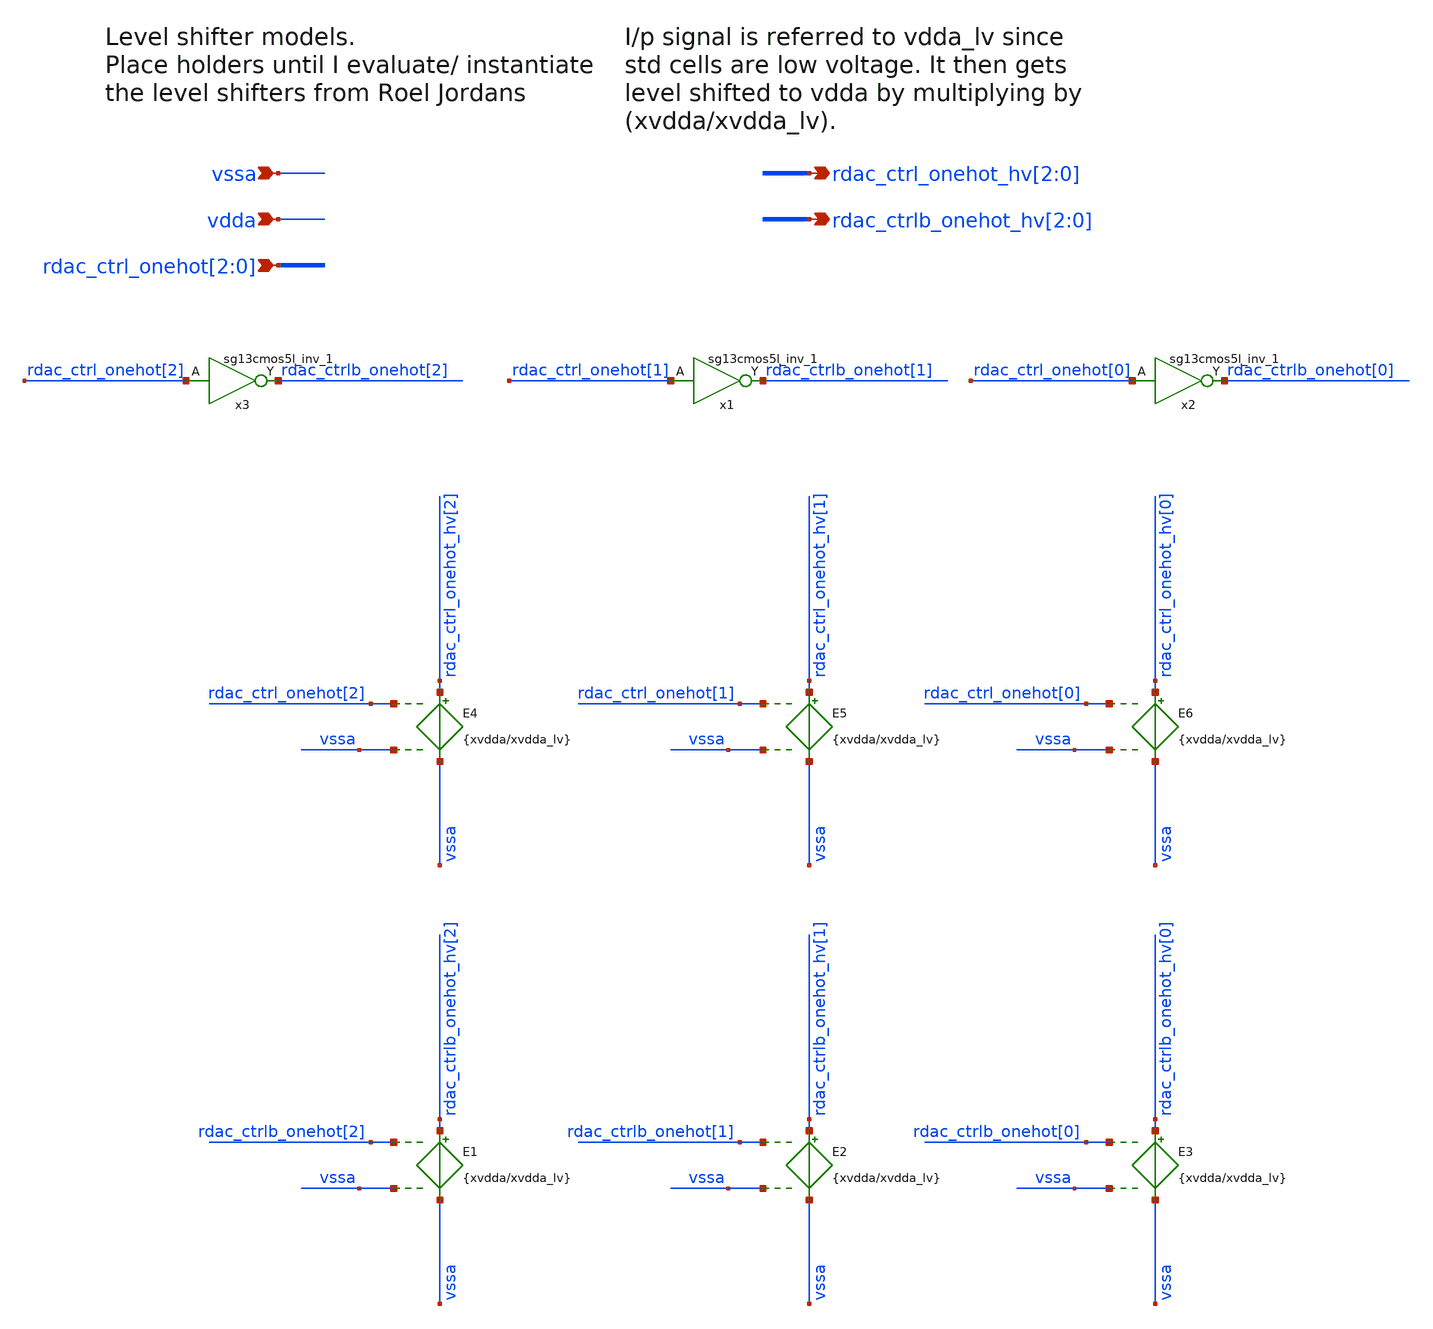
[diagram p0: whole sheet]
** sch_path: Design_Review_2/INA/Testbench_3_tb_sunrise_bias_ia_top_STEP_STB_NOISE/lvl_shfters.sch
**.subckt lvl_shfters rdac_ctrl_onehot[2],rdac_ctrl_onehot[1],rdac_ctrl_onehot[0] vssa
*+ rdac_ctrl_onehot_hv[2],rdac_ctrl_onehot_hv[1],rdac_ctrl_onehot_hv[0] rdac_ctrlb_onehot_hv[2],rdac_ctrlb_onehot_hv[1],rdac_ctrlb_onehot_hv[0] vdda
*.ipin rdac_ctrl_onehot[2],rdac_ctrl_onehot[1],rdac_ctrl_onehot[0]
*.ipin vssa
*.opin rdac_ctrl_onehot_hv[2],rdac_ctrl_onehot_hv[1],rdac_ctrl_onehot_hv[0]
*.opin rdac_ctrlb_onehot_hv[2],rdac_ctrlb_onehot_hv[1],rdac_ctrlb_onehot_hv[0]
*.ipin vdda
E1 rdac_ctrlb_onehot_hv[2] vssa rdac_ctrlb_onehot[2] vssa {xvdda/xvdda_lv}
E2 rdac_ctrlb_onehot_hv[1] vssa rdac_ctrlb_onehot[1] vssa {xvdda/xvdda_lv}
E3 rdac_ctrlb_onehot_hv[0] vssa rdac_ctrlb_onehot[0] vssa {xvdda/xvdda_lv}
E4 rdac_ctrl_onehot_hv[2] vssa rdac_ctrl_onehot[2] vssa {xvdda/xvdda_lv}
E5 rdac_ctrl_onehot_hv[1] vssa rdac_ctrl_onehot[1] vssa {xvdda/xvdda_lv}
E6 rdac_ctrl_onehot_hv[0] vssa rdac_ctrl_onehot[0] vssa {xvdda/xvdda_lv}
x3 rdac_ctrlb_onehot[2] rdac_ctrl_onehot[2] vdda vssa sg13cmos5l_inv_1
x1 rdac_ctrlb_onehot[1] rdac_ctrl_onehot[1] vdda vssa sg13cmos5l_inv_1
x2 rdac_ctrlb_onehot[0] rdac_ctrl_onehot[0] vdda vssa sg13cmos5l_inv_1
**.ends
.end
